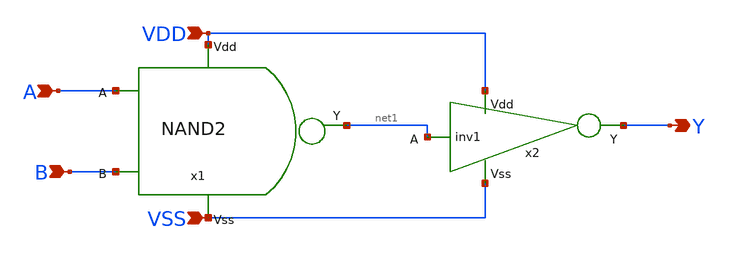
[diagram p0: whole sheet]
** sch_path: designs/libs/core_digital/schem/AND2.sch
**.subckt AND2 A B VSS VDD Y
*.ipin A
*.ipin B
*.ipin VSS
*.ipin VDD
*.opin Y
x1 VDD net1 A B VSS NAND2
x2 VDD net1 Y VSS inv1
**.ends
.end
